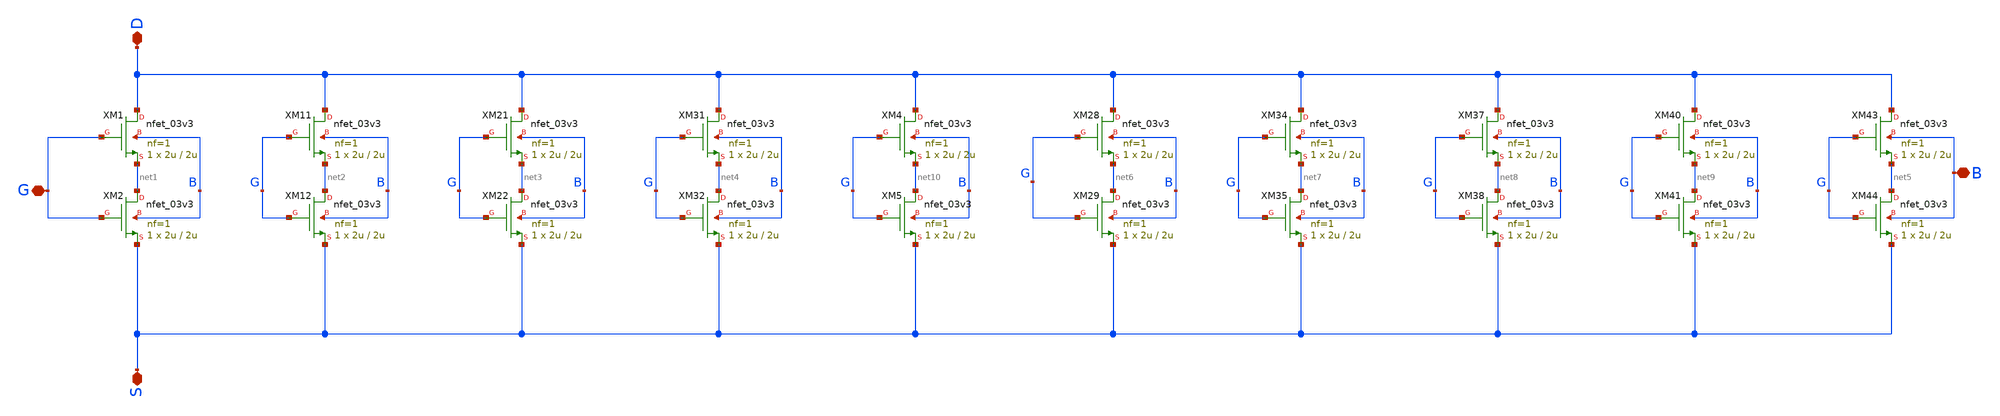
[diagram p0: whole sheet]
** sch_path: Voltage_Reference/symbols_vr/NMOS_matrix_VF.sch
**.subckt NMOS_matrix_VF D B G S
*.iopin D
*.iopin B
*.iopin G
*.iopin S
XM1 D G net1 B nfet_03v3 L=2u W=2u nf=1 ad='int((nf+1)/2) * W/nf * 0.18u' as='int((nf+2)/2) * W/nf * 0.18u'
+ pd='2*int((nf+1)/2) * (W/nf + 0.18u)' ps='2*int((nf+2)/2) * (W/nf + 0.18u)' nrd='0.18u / W' nrs='0.18u / W'
+ sa=0 sb=0 sd=0 m=1
XM2 net1 G S B nfet_03v3 L=2u W=2u nf=1 ad='int((nf+1)/2) * W/nf * 0.18u' as='int((nf+2)/2) * W/nf * 0.18u'
+ pd='2*int((nf+1)/2) * (W/nf + 0.18u)' ps='2*int((nf+2)/2) * (W/nf + 0.18u)' nrd='0.18u / W' nrs='0.18u / W'
+ sa=0 sb=0 sd=0 m=1
XM11 D G net2 B nfet_03v3 L=2u W=2u nf=1 ad='int((nf+1)/2) * W/nf * 0.18u' as='int((nf+2)/2) * W/nf * 0.18u'
+ pd='2*int((nf+1)/2) * (W/nf + 0.18u)' ps='2*int((nf+2)/2) * (W/nf + 0.18u)' nrd='0.18u / W' nrs='0.18u / W'
+ sa=0 sb=0 sd=0 m=1
XM12 net2 G S B nfet_03v3 L=2u W=2u nf=1 ad='int((nf+1)/2) * W/nf * 0.18u' as='int((nf+2)/2) * W/nf * 0.18u'
+ pd='2*int((nf+1)/2) * (W/nf + 0.18u)' ps='2*int((nf+2)/2) * (W/nf + 0.18u)' nrd='0.18u / W' nrs='0.18u / W'
+ sa=0 sb=0 sd=0 m=1
XM21 D G net3 B nfet_03v3 L=2u W=2u nf=1 ad='int((nf+1)/2) * W/nf * 0.18u' as='int((nf+2)/2) * W/nf * 0.18u'
+ pd='2*int((nf+1)/2) * (W/nf + 0.18u)' ps='2*int((nf+2)/2) * (W/nf + 0.18u)' nrd='0.18u / W' nrs='0.18u / W'
+ sa=0 sb=0 sd=0 m=1
XM22 net3 G S B nfet_03v3 L=2u W=2u nf=1 ad='int((nf+1)/2) * W/nf * 0.18u' as='int((nf+2)/2) * W/nf * 0.18u'
+ pd='2*int((nf+1)/2) * (W/nf + 0.18u)' ps='2*int((nf+2)/2) * (W/nf + 0.18u)' nrd='0.18u / W' nrs='0.18u / W'
+ sa=0 sb=0 sd=0 m=1
XM31 D G net4 B nfet_03v3 L=2u W=2u nf=1 ad='int((nf+1)/2) * W/nf * 0.18u' as='int((nf+2)/2) * W/nf * 0.18u'
+ pd='2*int((nf+1)/2) * (W/nf + 0.18u)' ps='2*int((nf+2)/2) * (W/nf + 0.18u)' nrd='0.18u / W' nrs='0.18u / W'
+ sa=0 sb=0 sd=0 m=1
XM32 net4 G S B nfet_03v3 L=2u W=2u nf=1 ad='int((nf+1)/2) * W/nf * 0.18u' as='int((nf+2)/2) * W/nf * 0.18u'
+ pd='2*int((nf+1)/2) * (W/nf + 0.18u)' ps='2*int((nf+2)/2) * (W/nf + 0.18u)' nrd='0.18u / W' nrs='0.18u / W'
+ sa=0 sb=0 sd=0 m=1
XM4 D G net10 B nfet_03v3 L=2u W=2u nf=1 ad='int((nf+1)/2) * W/nf * 0.18u' as='int((nf+2)/2) * W/nf * 0.18u'
+ pd='2*int((nf+1)/2) * (W/nf + 0.18u)' ps='2*int((nf+2)/2) * (W/nf + 0.18u)' nrd='0.18u / W' nrs='0.18u / W'
+ sa=0 sb=0 sd=0 m=1
XM5 net10 G S B nfet_03v3 L=2u W=2u nf=1 ad='int((nf+1)/2) * W/nf * 0.18u' as='int((nf+2)/2) * W/nf * 0.18u'
+ pd='2*int((nf+1)/2) * (W/nf + 0.18u)' ps='2*int((nf+2)/2) * (W/nf + 0.18u)' nrd='0.18u / W' nrs='0.18u / W'
+ sa=0 sb=0 sd=0 m=1
XM28 D G net6 B nfet_03v3 L=2u W=2u nf=1 ad='int((nf+1)/2) * W/nf * 0.18u' as='int((nf+2)/2) * W/nf * 0.18u'
+ pd='2*int((nf+1)/2) * (W/nf + 0.18u)' ps='2*int((nf+2)/2) * (W/nf + 0.18u)' nrd='0.18u / W' nrs='0.18u / W'
+ sa=0 sb=0 sd=0 m=1
XM29 net6 G S B nfet_03v3 L=2u W=2u nf=1 ad='int((nf+1)/2) * W/nf * 0.18u' as='int((nf+2)/2) * W/nf * 0.18u'
+ pd='2*int((nf+1)/2) * (W/nf + 0.18u)' ps='2*int((nf+2)/2) * (W/nf + 0.18u)' nrd='0.18u / W' nrs='0.18u / W'
+ sa=0 sb=0 sd=0 m=1
XM34 D G net7 B nfet_03v3 L=2u W=2u nf=1 ad='int((nf+1)/2) * W/nf * 0.18u' as='int((nf+2)/2) * W/nf * 0.18u'
+ pd='2*int((nf+1)/2) * (W/nf + 0.18u)' ps='2*int((nf+2)/2) * (W/nf + 0.18u)' nrd='0.18u / W' nrs='0.18u / W'
+ sa=0 sb=0 sd=0 m=1
XM35 net7 G S B nfet_03v3 L=2u W=2u nf=1 ad='int((nf+1)/2) * W/nf * 0.18u' as='int((nf+2)/2) * W/nf * 0.18u'
+ pd='2*int((nf+1)/2) * (W/nf + 0.18u)' ps='2*int((nf+2)/2) * (W/nf + 0.18u)' nrd='0.18u / W' nrs='0.18u / W'
+ sa=0 sb=0 sd=0 m=1
XM37 D G net8 B nfet_03v3 L=2u W=2u nf=1 ad='int((nf+1)/2) * W/nf * 0.18u' as='int((nf+2)/2) * W/nf * 0.18u'
+ pd='2*int((nf+1)/2) * (W/nf + 0.18u)' ps='2*int((nf+2)/2) * (W/nf + 0.18u)' nrd='0.18u / W' nrs='0.18u / W'
+ sa=0 sb=0 sd=0 m=1
XM38 net8 G S B nfet_03v3 L=2u W=2u nf=1 ad='int((nf+1)/2) * W/nf * 0.18u' as='int((nf+2)/2) * W/nf * 0.18u'
+ pd='2*int((nf+1)/2) * (W/nf + 0.18u)' ps='2*int((nf+2)/2) * (W/nf + 0.18u)' nrd='0.18u / W' nrs='0.18u / W'
+ sa=0 sb=0 sd=0 m=1
XM40 D G net9 B nfet_03v3 L=2u W=2u nf=1 ad='int((nf+1)/2) * W/nf * 0.18u' as='int((nf+2)/2) * W/nf * 0.18u'
+ pd='2*int((nf+1)/2) * (W/nf + 0.18u)' ps='2*int((nf+2)/2) * (W/nf + 0.18u)' nrd='0.18u / W' nrs='0.18u / W'
+ sa=0 sb=0 sd=0 m=1
XM41 net9 G S B nfet_03v3 L=2u W=2u nf=1 ad='int((nf+1)/2) * W/nf * 0.18u' as='int((nf+2)/2) * W/nf * 0.18u'
+ pd='2*int((nf+1)/2) * (W/nf + 0.18u)' ps='2*int((nf+2)/2) * (W/nf + 0.18u)' nrd='0.18u / W' nrs='0.18u / W'
+ sa=0 sb=0 sd=0 m=1
XM43 D G net5 B nfet_03v3 L=2u W=2u nf=1 ad='int((nf+1)/2) * W/nf * 0.18u' as='int((nf+2)/2) * W/nf * 0.18u'
+ pd='2*int((nf+1)/2) * (W/nf + 0.18u)' ps='2*int((nf+2)/2) * (W/nf + 0.18u)' nrd='0.18u / W' nrs='0.18u / W'
+ sa=0 sb=0 sd=0 m=1
XM44 net5 G S B nfet_03v3 L=2u W=2u nf=1 ad='int((nf+1)/2) * W/nf * 0.18u' as='int((nf+2)/2) * W/nf * 0.18u'
+ pd='2*int((nf+1)/2) * (W/nf + 0.18u)' ps='2*int((nf+2)/2) * (W/nf + 0.18u)' nrd='0.18u / W' nrs='0.18u / W'
+ sa=0 sb=0 sd=0 m=1
**.ends
.end
